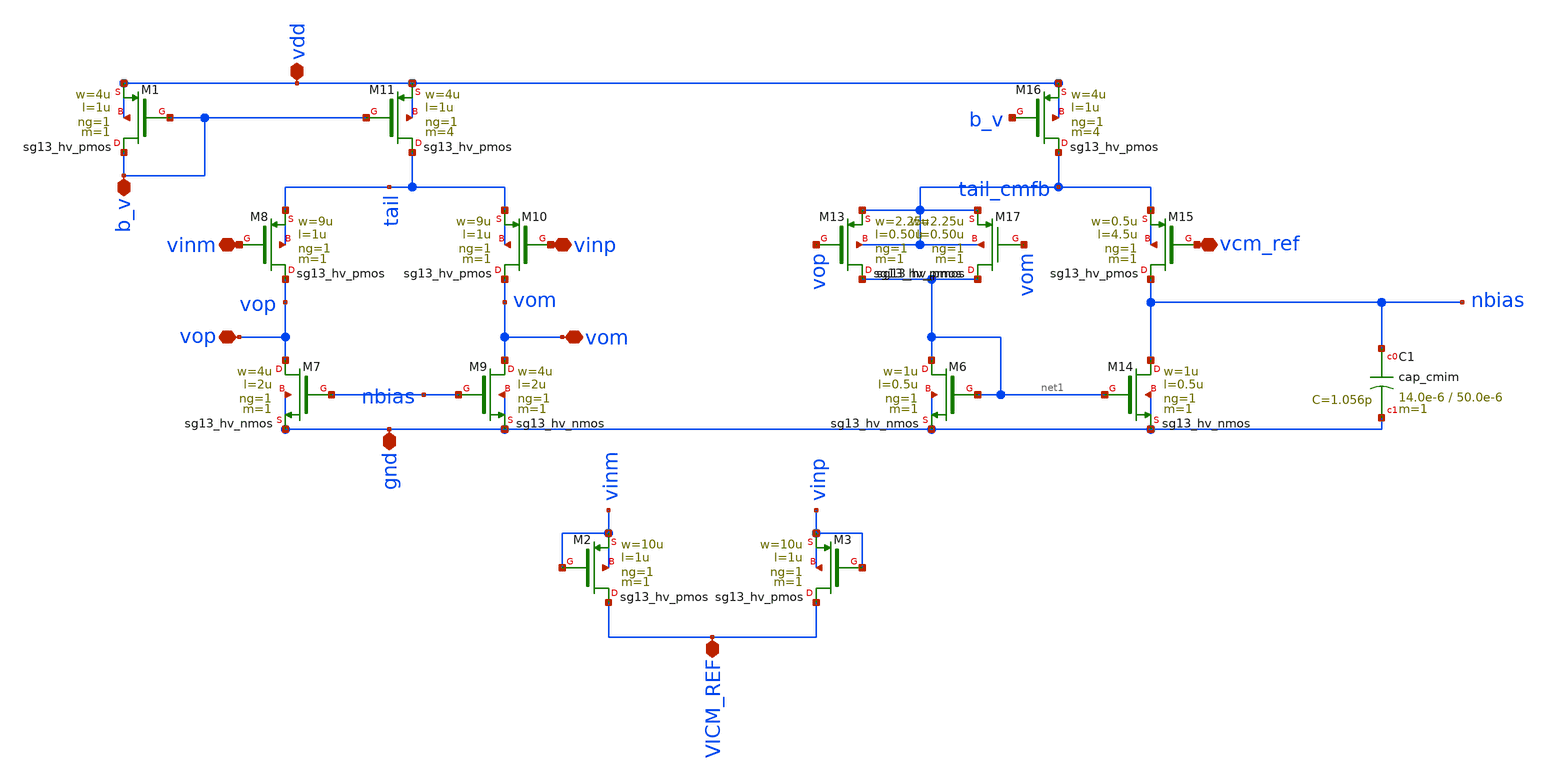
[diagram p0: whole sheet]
** sch_path: Differntial_ended_symbol_making.sch
**.subckt Differntial_ended_symbol_making b_v vinm vcm_ref vinp vop vom gnd vdd VICM_REF
*.iopin b_v
*.iopin vinm
*.iopin vcm_ref
*.iopin vinp
*.iopin vop
*.iopin vom
*.iopin gnd
*.iopin vdd
*.iopin VICM_REF
XM7 vop nbias gnd gnd sg13_hv_nmos w=4u l=2u ng=1 m=1 mm_ok=1
XM8 vop vinm tail tail sg13_hv_pmos w=9u l=1u ng=1 m=1 mm_ok=1
XM9 vom nbias gnd gnd sg13_hv_nmos w=4u l=2u ng=1 m=1 mm_ok=1
XM10 vom vinp tail tail sg13_hv_pmos w=9u l=1u ng=1 m=1 mm_ok=1
XM11 tail b_v vdd vdd sg13_hv_pmos w=4u l=1u ng=1 m=4 mm_ok=1
XM6 net1 net1 gnd gnd sg13_hv_nmos w=1u l=0.5u ng=1 m=1 mm_ok=1
XM13 net1 vop tail_cmfb tail_cmfb sg13_hv_pmos w=2.25u l=0.50u ng=1 m=1 mm_ok=1
XM14 nbias net1 gnd gnd sg13_hv_nmos w=1u l=0.5u ng=1 m=1 mm_ok=1
XM15 nbias vcm_ref tail_cmfb tail_cmfb sg13_hv_pmos w=0.5u l=4.5u ng=1 m=1 mm_ok=1
XM16 tail_cmfb b_v vdd vdd sg13_hv_pmos w=4u l=1u ng=1 m=4 mm_ok=1
XM17 net1 vom tail_cmfb tail_cmfb sg13_hv_pmos w=2.25u l=0.50u ng=1 m=1 mm_ok=1
XM1 b_v b_v vdd vdd sg13_hv_pmos w=4u l=1u ng=1 m=1 mm_ok=1
XC1 nbias gnd cap_cmim w=14.0e-6 l=50.0e-6 m=1 mm_ok=1
XM2 VICM_REF vinm vinm vinm sg13_hv_pmos w=10u l=1u ng=1 m=1 mm_ok=1
XM3 VICM_REF vinp vinp vinp sg13_hv_pmos w=10u l=1u ng=1 m=1 mm_ok=1
**.ends
.end
